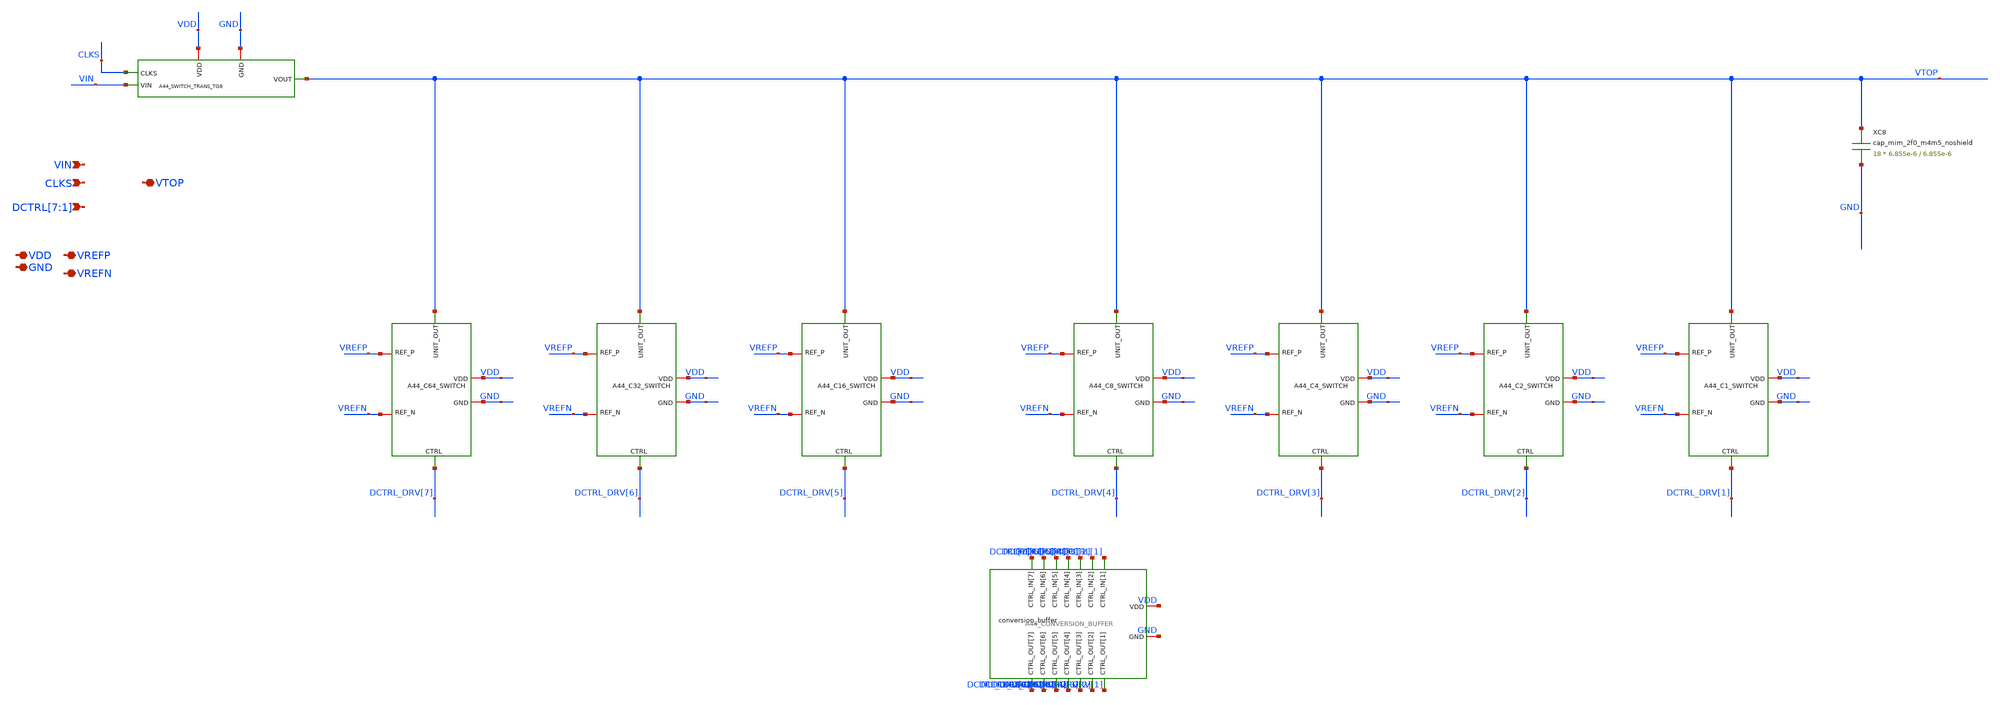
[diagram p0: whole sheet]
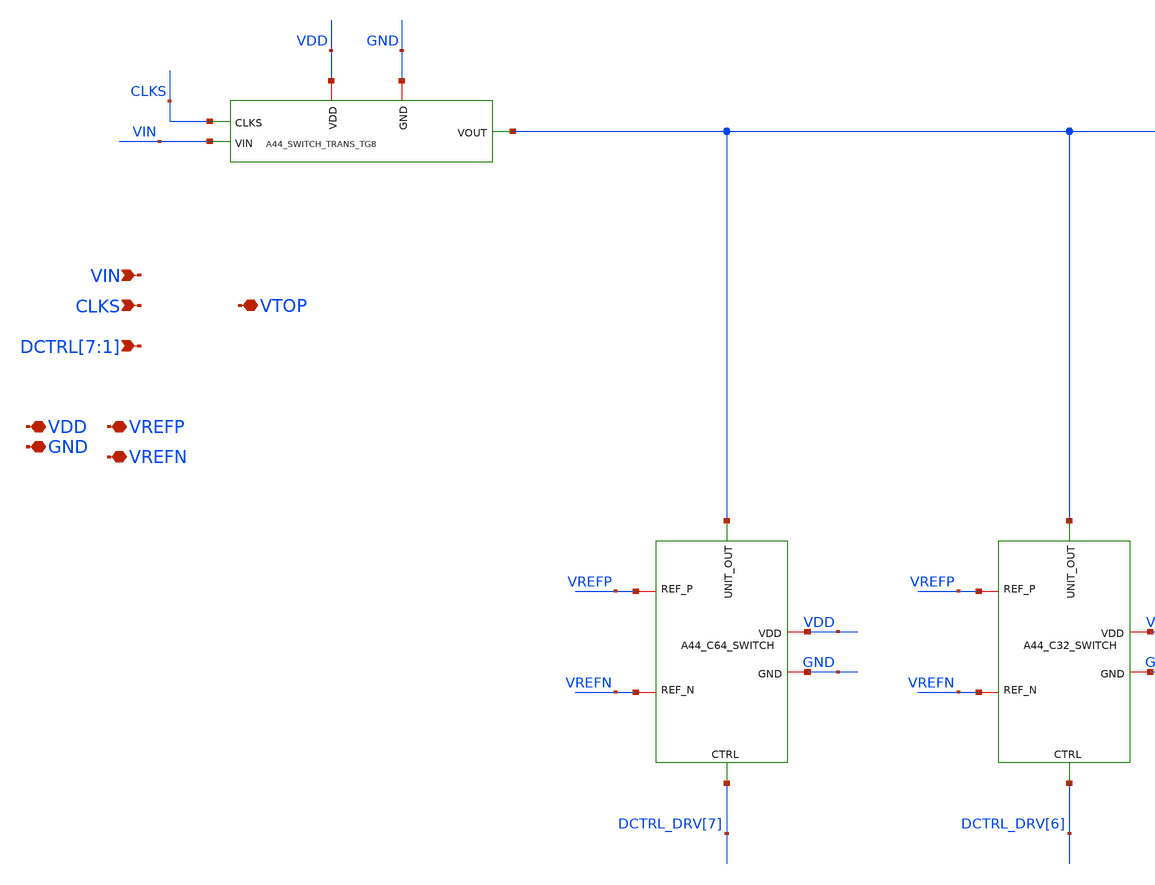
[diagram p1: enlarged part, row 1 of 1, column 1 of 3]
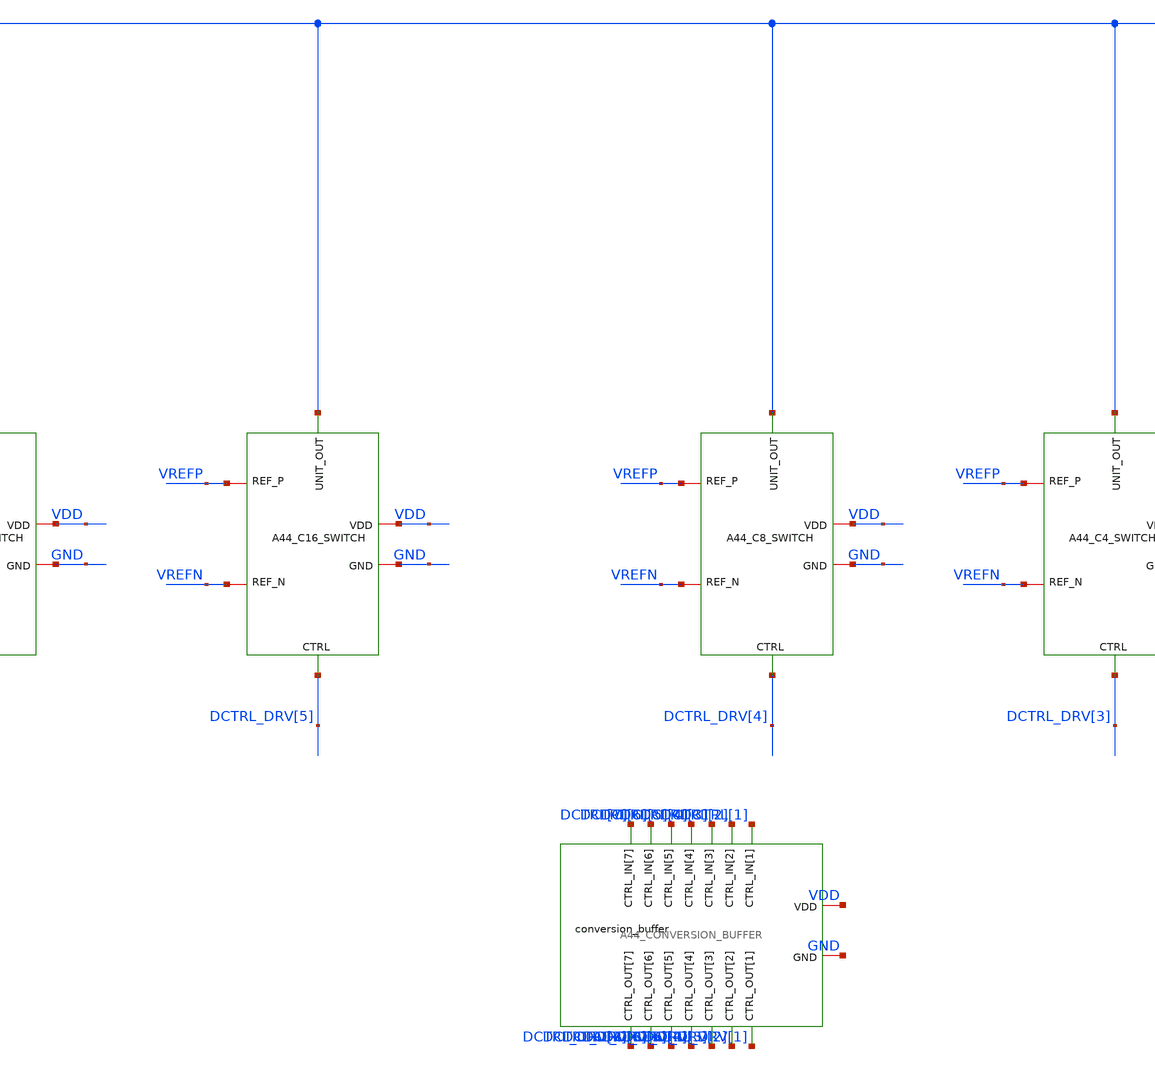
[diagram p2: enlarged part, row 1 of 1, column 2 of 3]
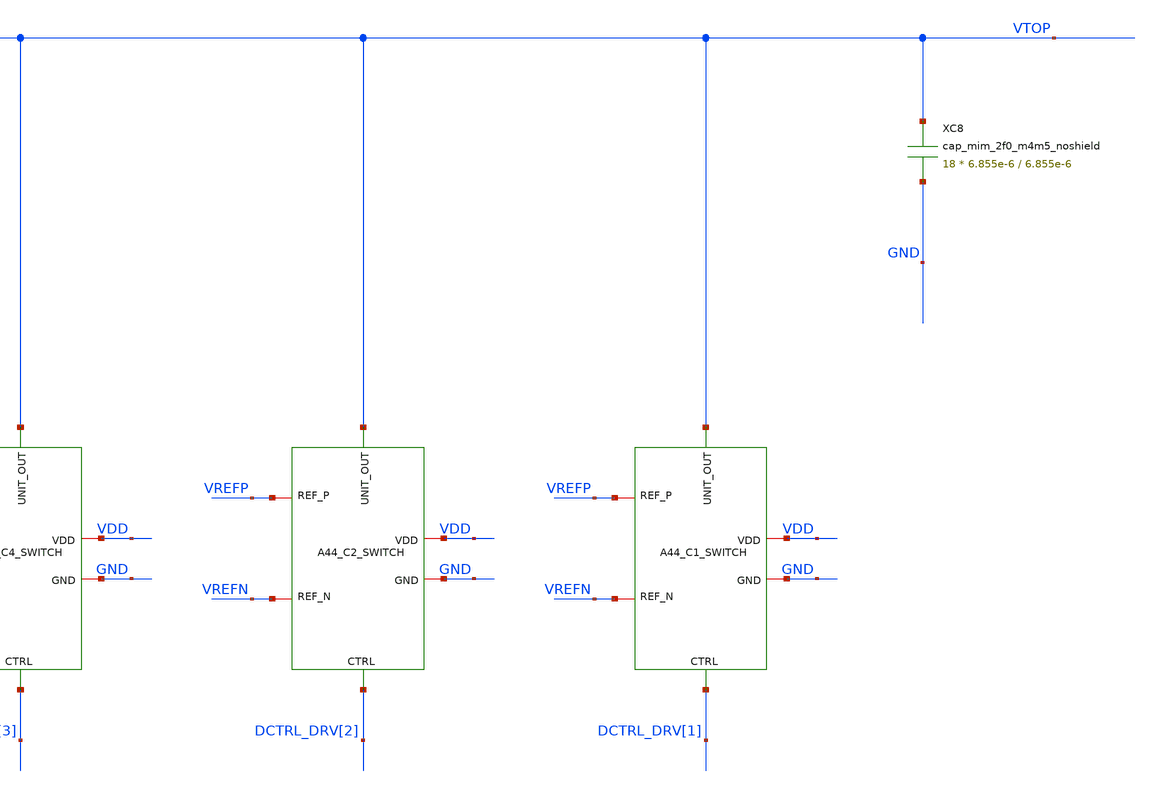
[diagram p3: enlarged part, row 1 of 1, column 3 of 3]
** sch_path: verification/a44_w5p29_trans_driver/01_CURRENT_CIRCUIT_FILES/xschem/A44_CDAC_UNIT_TRANS_DRIVER.sch
**.subckt A44_CDAC_UNIT_TRANS_DRIVER VIN CLKS VDD GND VREFP VREFN VTOP
*+ DCTRL[7],DCTRL[6],DCTRL[5],DCTRL[4],DCTRL[3],DCTRL[2],DCTRL[1]
*.ipin VIN
*.ipin CLKS
*.iopin VDD
*.iopin GND
*.iopin VREFP
*.iopin VREFN
*.iopin VTOP
*.ipin DCTRL[7],DCTRL[6],DCTRL[5],DCTRL[4],DCTRL[3],DCTRL[2],DCTRL[1]
XC8 VTOP GND cap_mim_2f0_m4m5_noshield c_width=6.855e-6 c_length=6.855e-6 m=18
x2 VREFN VREFP VDD GND VTOP DCTRL_DRV[1] A44_C1_SWITCH
x3 VREFN VREFP VDD GND VTOP DCTRL_DRV[2] A44_C2_SWITCH
x4 VREFN VREFP VDD GND VTOP DCTRL_DRV[3] A44_C4_SWITCH
x5 VREFN VREFP VDD GND VTOP DCTRL_DRV[4] A44_C8_SWITCH
x6 VREFN VREFP VDD GND VTOP DCTRL_DRV[5] A44_C16_SWITCH
x8 VREFN VREFP VDD GND VTOP DCTRL_DRV[7] A44_C64_SWITCH
xsample CLKS VDD GND VTOP VIN A44_SWITCH_TRANS_TG8
x1 VREFN VREFP VDD GND VTOP DCTRL_DRV[6] A44_C32_SWITCH
xdrv DCTRL[1] DCTRL_DRV[1] VDD GND DCTRL[2] DCTRL_DRV[2] DCTRL_DRV[3] DCTRL[3] DCTRL_DRV[4] DCTRL[4]
+ DCTRL_DRV[5] DCTRL[5] DCTRL_DRV[6] DCTRL[6] DCTRL_DRV[7] DCTRL[7] A44_CONVERSION_BUFFER
**.ends

* expanding   symbol:  A44_C1_SWITCH.sym # of pins=6
** sym_path: verification/a44_w5p29_trans_driver/01_CURRENT_CIRCUIT_FILES/xschem/A44_C1_SWITCH.sym
** sch_path: verification/a44_w5p29_trans_driver/01_CURRENT_CIRCUIT_FILES/xschem/A44_C1_SWITCH.sch
.subckt A44_C1_SWITCH REF_N REF_P VDD GND UNIT_OUT CTRL
*.iopin REF_N
*.iopin REF_P
*.iopin VDD
*.iopin GND
*.ipin CTRL
*.opin UNIT_OUT
x1 REF_P REF_N CTRL V_BOT VDD GND A44_CAP_SWITCH
XC1 UNIT_OUT V_BOT cap_mim_2f0_m4m5_noshield c_width=6.855e-6 c_length=6.855e-6 m=18
.ends


* expanding   symbol:  A44_C2_SWITCH.sym # of pins=6
** sym_path: verification/a44_w5p29_trans_driver/01_CURRENT_CIRCUIT_FILES/xschem/A44_C2_SWITCH.sym
** sch_path: verification/a44_w5p29_trans_driver/01_CURRENT_CIRCUIT_FILES/xschem/A44_C2_SWITCH.sch
.subckt A44_C2_SWITCH REF_N REF_P VDD GND UNIT_OUT CTRL
*.iopin REF_N
*.iopin REF_P
*.iopin VDD
*.iopin GND
*.ipin CTRL
*.opin UNIT_OUT
x1 REF_N REF_P VDD GND UNIT_OUT CTRL A44_C1_SWITCH
x2 REF_N REF_P VDD GND UNIT_OUT CTRL A44_C1_SWITCH
.ends


* expanding   symbol:  A44_C4_SWITCH.sym # of pins=6
** sym_path: verification/a44_w5p29_trans_driver/01_CURRENT_CIRCUIT_FILES/xschem/A44_C4_SWITCH.sym
** sch_path: verification/a44_w5p29_trans_driver/01_CURRENT_CIRCUIT_FILES/xschem/A44_C4_SWITCH.sch
.subckt A44_C4_SWITCH REF_N REF_P VDD GND UNIT_OUT CTRL
*.iopin REF_N
*.iopin REF_P
*.iopin VDD
*.iopin GND
*.ipin CTRL
*.opin UNIT_OUT
x1 REF_N REF_P VDD GND UNIT_OUT CTRL A44_C1_SWITCH
x2 REF_N REF_P VDD GND UNIT_OUT CTRL A44_C1_SWITCH
x3 REF_N REF_P VDD GND UNIT_OUT CTRL A44_C1_SWITCH
x4 REF_N REF_P VDD GND UNIT_OUT CTRL A44_C1_SWITCH
.ends


* expanding   symbol:  A44_C8_SWITCH.sym # of pins=6
** sym_path: verification/a44_w5p29_trans_driver/01_CURRENT_CIRCUIT_FILES/xschem/A44_C8_SWITCH.sym
** sch_path: verification/a44_w5p29_trans_driver/01_CURRENT_CIRCUIT_FILES/xschem/A44_C8_SWITCH.sch
.subckt A44_C8_SWITCH REF_N REF_P VDD GND UNIT_OUT CTRL
*.iopin REF_N
*.iopin REF_P
*.iopin VDD
*.iopin GND
*.ipin CTRL
*.opin UNIT_OUT
x1 REF_N REF_P VDD GND UNIT_OUT CTRL A44_C1_SWITCH
x2 REF_N REF_P VDD GND UNIT_OUT CTRL A44_C1_SWITCH
x3 REF_N REF_P VDD GND UNIT_OUT CTRL A44_C1_SWITCH
x4 REF_N REF_P VDD GND UNIT_OUT CTRL A44_C1_SWITCH
x5 REF_N REF_P VDD GND UNIT_OUT CTRL A44_C1_SWITCH
x6 REF_N REF_P VDD GND UNIT_OUT CTRL A44_C1_SWITCH
x7 REF_N REF_P VDD GND UNIT_OUT CTRL A44_C1_SWITCH
x8 REF_N REF_P VDD GND UNIT_OUT CTRL A44_C1_SWITCH
.ends


* expanding   symbol:  A44_C16_SWITCH.sym # of pins=6
** sym_path: verification/a44_w5p29_trans_driver/01_CURRENT_CIRCUIT_FILES/xschem/A44_C16_SWITCH.sym
** sch_path: verification/a44_w5p29_trans_driver/01_CURRENT_CIRCUIT_FILES/xschem/A44_C16_SWITCH.sch
.subckt A44_C16_SWITCH REF_N REF_P VDD GND UNIT_OUT CTRL
*.iopin REF_N
*.iopin REF_P
*.iopin VDD
*.iopin GND
*.ipin CTRL
*.opin UNIT_OUT
x1 REF_N REF_P VDD GND UNIT_OUT CTRL A44_C1_SWITCH
x2 REF_N REF_P VDD GND UNIT_OUT CTRL A44_C1_SWITCH
x3 REF_N REF_P VDD GND UNIT_OUT CTRL A44_C1_SWITCH
x4 REF_N REF_P VDD GND UNIT_OUT CTRL A44_C1_SWITCH
x5 REF_N REF_P VDD GND UNIT_OUT CTRL A44_C1_SWITCH
x6 REF_N REF_P VDD GND UNIT_OUT CTRL A44_C1_SWITCH
x7 REF_N REF_P VDD GND UNIT_OUT CTRL A44_C1_SWITCH
x8 REF_N REF_P VDD GND UNIT_OUT CTRL A44_C1_SWITCH
x9 REF_N REF_P VDD GND UNIT_OUT CTRL A44_C1_SWITCH
x10 REF_N REF_P VDD GND UNIT_OUT CTRL A44_C1_SWITCH
x11 REF_N REF_P VDD GND UNIT_OUT CTRL A44_C1_SWITCH
x12 REF_N REF_P VDD GND UNIT_OUT CTRL A44_C1_SWITCH
x13 REF_N REF_P VDD GND UNIT_OUT CTRL A44_C1_SWITCH
x14 REF_N REF_P VDD GND UNIT_OUT CTRL A44_C1_SWITCH
x15 REF_N REF_P VDD GND UNIT_OUT CTRL A44_C1_SWITCH
x16 REF_N REF_P VDD GND UNIT_OUT CTRL A44_C1_SWITCH
.ends


* expanding   symbol:  A44_C64_SWITCH.sym # of pins=6
** sym_path: verification/a44_w5p29_trans_driver/01_CURRENT_CIRCUIT_FILES/xschem/A44_C64_SWITCH.sym
** sch_path: verification/a44_w5p29_trans_driver/01_CURRENT_CIRCUIT_FILES/xschem/A44_C64_SWITCH.sch
.subckt A44_C64_SWITCH REF_N REF_P VDD GND UNIT_OUT CTRL
*.iopin REF_N
*.iopin REF_P
*.iopin VDD
*.iopin GND
*.ipin CTRL
*.opin UNIT_OUT
x1 REF_N REF_P VDD GND UNIT_OUT CTRL A44_C1_SWITCH
x2 REF_N REF_P VDD GND UNIT_OUT CTRL A44_C1_SWITCH
x3 REF_N REF_P VDD GND UNIT_OUT CTRL A44_C1_SWITCH
x4 REF_N REF_P VDD GND UNIT_OUT CTRL A44_C1_SWITCH
x5 REF_N REF_P VDD GND UNIT_OUT CTRL A44_C1_SWITCH
x6 REF_N REF_P VDD GND UNIT_OUT CTRL A44_C1_SWITCH
x7 REF_N REF_P VDD GND UNIT_OUT CTRL A44_C1_SWITCH
x8 REF_N REF_P VDD GND UNIT_OUT CTRL A44_C1_SWITCH
x9 REF_N REF_P VDD GND UNIT_OUT CTRL A44_C1_SWITCH
x10 REF_N REF_P VDD GND UNIT_OUT CTRL A44_C1_SWITCH
x11 REF_N REF_P VDD GND UNIT_OUT CTRL A44_C1_SWITCH
x12 REF_N REF_P VDD GND UNIT_OUT CTRL A44_C1_SWITCH
x13 REF_N REF_P VDD GND UNIT_OUT CTRL A44_C1_SWITCH
x14 REF_N REF_P VDD GND UNIT_OUT CTRL A44_C1_SWITCH
x15 REF_N REF_P VDD GND UNIT_OUT CTRL A44_C1_SWITCH
x16 REF_N REF_P VDD GND UNIT_OUT CTRL A44_C1_SWITCH
x17 REF_N REF_P VDD GND UNIT_OUT CTRL A44_C1_SWITCH
x18 REF_N REF_P VDD GND UNIT_OUT CTRL A44_C1_SWITCH
x19 REF_N REF_P VDD GND UNIT_OUT CTRL A44_C1_SWITCH
x20 REF_N REF_P VDD GND UNIT_OUT CTRL A44_C1_SWITCH
x21 REF_N REF_P VDD GND UNIT_OUT CTRL A44_C1_SWITCH
x22 REF_N REF_P VDD GND UNIT_OUT CTRL A44_C1_SWITCH
x23 REF_N REF_P VDD GND UNIT_OUT CTRL A44_C1_SWITCH
x24 REF_N REF_P VDD GND UNIT_OUT CTRL A44_C1_SWITCH
x25 REF_N REF_P VDD GND UNIT_OUT CTRL A44_C1_SWITCH
x26 REF_N REF_P VDD GND UNIT_OUT CTRL A44_C1_SWITCH
x27 REF_N REF_P VDD GND UNIT_OUT CTRL A44_C1_SWITCH
x28 REF_N REF_P VDD GND UNIT_OUT CTRL A44_C1_SWITCH
x29 REF_N REF_P VDD GND UNIT_OUT CTRL A44_C1_SWITCH
x30 REF_N REF_P VDD GND UNIT_OUT CTRL A44_C1_SWITCH
x31 REF_N REF_P VDD GND UNIT_OUT CTRL A44_C1_SWITCH
x32 REF_N REF_P VDD GND UNIT_OUT CTRL A44_C1_SWITCH
x33 REF_N REF_P VDD GND UNIT_OUT CTRL A44_C1_SWITCH
x34 REF_N REF_P VDD GND UNIT_OUT CTRL A44_C1_SWITCH
x35 REF_N REF_P VDD GND UNIT_OUT CTRL A44_C1_SWITCH
x36 REF_N REF_P VDD GND UNIT_OUT CTRL A44_C1_SWITCH
x37 REF_N REF_P VDD GND UNIT_OUT CTRL A44_C1_SWITCH
x38 REF_N REF_P VDD GND UNIT_OUT CTRL A44_C1_SWITCH
x39 REF_N REF_P VDD GND UNIT_OUT CTRL A44_C1_SWITCH
x40 REF_N REF_P VDD GND UNIT_OUT CTRL A44_C1_SWITCH
x41 REF_N REF_P VDD GND UNIT_OUT CTRL A44_C1_SWITCH
x42 REF_N REF_P VDD GND UNIT_OUT CTRL A44_C1_SWITCH
x43 REF_N REF_P VDD GND UNIT_OUT CTRL A44_C1_SWITCH
x44 REF_N REF_P VDD GND UNIT_OUT CTRL A44_C1_SWITCH
x45 REF_N REF_P VDD GND UNIT_OUT CTRL A44_C1_SWITCH
x46 REF_N REF_P VDD GND UNIT_OUT CTRL A44_C1_SWITCH
x47 REF_N REF_P VDD GND UNIT_OUT CTRL A44_C1_SWITCH
x48 REF_N REF_P VDD GND UNIT_OUT CTRL A44_C1_SWITCH
x49 REF_N REF_P VDD GND UNIT_OUT CTRL A44_C1_SWITCH
x50 REF_N REF_P VDD GND UNIT_OUT CTRL A44_C1_SWITCH
x51 REF_N REF_P VDD GND UNIT_OUT CTRL A44_C1_SWITCH
x52 REF_N REF_P VDD GND UNIT_OUT CTRL A44_C1_SWITCH
x53 REF_N REF_P VDD GND UNIT_OUT CTRL A44_C1_SWITCH
x54 REF_N REF_P VDD GND UNIT_OUT CTRL A44_C1_SWITCH
x55 REF_N REF_P VDD GND UNIT_OUT CTRL A44_C1_SWITCH
x56 REF_N REF_P VDD GND UNIT_OUT CTRL A44_C1_SWITCH
x57 REF_N REF_P VDD GND UNIT_OUT CTRL A44_C1_SWITCH
x58 REF_N REF_P VDD GND UNIT_OUT CTRL A44_C1_SWITCH
x59 REF_N REF_P VDD GND UNIT_OUT CTRL A44_C1_SWITCH
x60 REF_N REF_P VDD GND UNIT_OUT CTRL A44_C1_SWITCH
x61 REF_N REF_P VDD GND UNIT_OUT CTRL A44_C1_SWITCH
x62 REF_N REF_P VDD GND UNIT_OUT CTRL A44_C1_SWITCH
x63 REF_N REF_P VDD GND UNIT_OUT CTRL A44_C1_SWITCH
x64 REF_N REF_P VDD GND UNIT_OUT CTRL A44_C1_SWITCH
.ends


* expanding   symbol:  A44_SWITCH_TRANS_TG8.sym # of pins=5
** sym_path: verification/a44_w5p29_trans_driver/01_CURRENT_CIRCUIT_FILES/xschem/A44_SWITCH_TRANS_TG8.sym
** sch_path: verification/a44_w5p29_trans_driver/01_CURRENT_CIRCUIT_FILES/xschem/A44_SWITCH_TRANS_TG8.sch
.subckt A44_SWITCH_TRANS_TG8 CLKS VDD GND VOUT VIN
*.iopin VDD
*.iopin GND
*.ipin VIN
*.ipin CLKS
*.opin VOUT
XTG_CLK_INV1_NMOS net1 CLKS GND GND nfet_03v3 L=0.28u W=1.56u nf=1 ad='int((nf+1)/2) * W/nf * 0.18u'
+ as='int((nf+2)/2) * W/nf * 0.18u' pd='2*int((nf+1)/2) * (W/nf + 0.18u)' ps='2*int((nf+2)/2) * (W/nf + 0.18u)'
+ nrd='0.18u / W' nrs='0.18u / W' sa=0 sb=0 sd=0 m=1
XTG_CLK_INV1_PMOS net1 CLKS VDD VDD pfet_03v3 L=0.28u W=3.11u nf=1 ad='int((nf+1)/2) * W/nf * 0.18u'
+ as='int((nf+2)/2) * W/nf * 0.18u' pd='2*int((nf+1)/2) * (W/nf + 0.18u)' ps='2*int((nf+2)/2) * (W/nf + 0.18u)'
+ nrd='0.18u / W' nrs='0.18u / W' sa=0 sb=0 sd=0 m=1
XTG_CLK_INV2_NMOS net2 net1 GND GND nfet_03v3 L=0.28u W=2.34u nf=1 ad='int((nf+1)/2) * W/nf * 0.18u'
+ as='int((nf+2)/2) * W/nf * 0.18u' pd='2*int((nf+1)/2) * (W/nf + 0.18u)' ps='2*int((nf+2)/2) * (W/nf + 0.18u)'
+ nrd='0.18u / W' nrs='0.18u / W' sa=0 sb=0 sd=0 m=1
XTG_CLK_INV2_PMOS net2 net1 VDD VDD pfet_03v3 L=0.28u W=4.67u nf=1 ad='int((nf+1)/2) * W/nf * 0.18u'
+ as='int((nf+2)/2) * W/nf * 0.18u' pd='2*int((nf+1)/2) * (W/nf + 0.18u)' ps='2*int((nf+2)/2) * (W/nf + 0.18u)'
+ nrd='0.18u / W' nrs='0.18u / W' sa=0 sb=0 sd=0 m=1
XTG_CLK_INV3_NMOS net3 net2 GND GND nfet_03v3 L=0.28u W=3.11u nf=1 ad='int((nf+1)/2) * W/nf * 0.18u'
+ as='int((nf+2)/2) * W/nf * 0.18u' pd='2*int((nf+1)/2) * (W/nf + 0.18u)' ps='2*int((nf+2)/2) * (W/nf + 0.18u)'
+ nrd='0.18u / W' nrs='0.18u / W' sa=0 sb=0 sd=0 m=1
XTG_CLK_INV3_PMOS net3 net2 VDD VDD pfet_03v3 L=0.28u W=6.22u nf=1 ad='int((nf+1)/2) * W/nf * 0.18u'
+ as='int((nf+2)/2) * W/nf * 0.18u' pd='2*int((nf+1)/2) * (W/nf + 0.18u)' ps='2*int((nf+2)/2) * (W/nf + 0.18u)'
+ nrd='0.18u / W' nrs='0.18u / W' sa=0 sb=0 sd=0 m=1
XTG_CLK_INV4_NMOS N_CLK net3 GND GND nfet_03v3 L=0.28u W=4.67u nf=1 ad='int((nf+1)/2) * W/nf * 0.18u'
+ as='int((nf+2)/2) * W/nf * 0.18u' pd='2*int((nf+1)/2) * (W/nf + 0.18u)' ps='2*int((nf+2)/2) * (W/nf + 0.18u)'
+ nrd='0.18u / W' nrs='0.18u / W' sa=0 sb=0 sd=0 m=1
XTG_CLK_INV4_PMOS N_CLK net3 VDD VDD pfet_03v3 L=0.28u W=9.33u nf=1 ad='int((nf+1)/2) * W/nf * 0.18u'
+ as='int((nf+2)/2) * W/nf * 0.18u' pd='2*int((nf+1)/2) * (W/nf + 0.18u)' ps='2*int((nf+2)/2) * (W/nf + 0.18u)'
+ nrd='0.18u / W' nrs='0.18u / W' sa=0 sb=0 sd=0 m=1
XTG_PCLK_INV1_NMOS net4 CLKS GND GND nfet_03v3 L=0.28u W=1.56u nf=1 ad='int((nf+1)/2) * W/nf * 0.18u'
+ as='int((nf+2)/2) * W/nf * 0.18u' pd='2*int((nf+1)/2) * (W/nf + 0.18u)' ps='2*int((nf+2)/2) * (W/nf + 0.18u)'
+ nrd='0.18u / W' nrs='0.18u / W' sa=0 sb=0 sd=0 m=1
XTG_PCLK_INV1_PMOS net4 CLKS VDD VDD pfet_03v3 L=0.28u W=3.11u nf=1 ad='int((nf+1)/2) * W/nf * 0.18u'
+ as='int((nf+2)/2) * W/nf * 0.18u' pd='2*int((nf+1)/2) * (W/nf + 0.18u)' ps='2*int((nf+2)/2) * (W/nf + 0.18u)'
+ nrd='0.18u / W' nrs='0.18u / W' sa=0 sb=0 sd=0 m=1
XTG_PCLK_INV2_NMOS net5 net4 GND GND nfet_03v3 L=0.28u W=3.11u nf=1 ad='int((nf+1)/2) * W/nf * 0.18u'
+ as='int((nf+2)/2) * W/nf * 0.18u' pd='2*int((nf+1)/2) * (W/nf + 0.18u)' ps='2*int((nf+2)/2) * (W/nf + 0.18u)'
+ nrd='0.18u / W' nrs='0.18u / W' sa=0 sb=0 sd=0 m=1
XTG_PCLK_INV2_PMOS net5 net4 VDD VDD pfet_03v3 L=0.28u W=6.22u nf=1 ad='int((nf+1)/2) * W/nf * 0.18u'
+ as='int((nf+2)/2) * W/nf * 0.18u' pd='2*int((nf+1)/2) * (W/nf + 0.18u)' ps='2*int((nf+2)/2) * (W/nf + 0.18u)'
+ nrd='0.18u / W' nrs='0.18u / W' sa=0 sb=0 sd=0 m=1
XTG_PCLK_INV3_NMOS P_CLK net5 GND GND nfet_03v3 L=0.28u W=6.22u nf=1 ad='int((nf+1)/2) * W/nf * 0.18u'
+ as='int((nf+2)/2) * W/nf * 0.18u' pd='2*int((nf+1)/2) * (W/nf + 0.18u)' ps='2*int((nf+2)/2) * (W/nf + 0.18u)'
+ nrd='0.18u / W' nrs='0.18u / W' sa=0 sb=0 sd=0 m=1
XTG_PCLK_INV3_PMOS P_CLK net5 VDD VDD pfet_03v3 L=0.28u W=12.44u nf=1 ad='int((nf+1)/2) * W/nf * 0.18u'
+ as='int((nf+2)/2) * W/nf * 0.18u' pd='2*int((nf+1)/2) * (W/nf + 0.18u)' ps='2*int((nf+2)/2) * (W/nf + 0.18u)'
+ nrd='0.18u / W' nrs='0.18u / W' sa=0 sb=0 sd=0 m=1
XTG_TRANS_NMOS VIN N_CLK VOUT GND nfet_03v3 L=0.28u W=3.11u nf=1 ad='int((nf+1)/2) * W/nf * 0.18u' as='int((nf+2)/2) * W/nf * 0.18u'
+ pd='2*int((nf+1)/2) * (W/nf + 0.18u)' ps='2*int((nf+2)/2) * (W/nf + 0.18u)' nrd='0.18u / W' nrs='0.18u / W'
+ sa=0 sb=0 sd=0 m=8
XTG_TRANS_PMOS VIN P_CLK VOUT VDD pfet_03v3 L=0.28u W=6.22u nf=1 ad='int((nf+1)/2) * W/nf * 0.18u' as='int((nf+2)/2) * W/nf * 0.18u'
+ pd='2*int((nf+1)/2) * (W/nf + 0.18u)' ps='2*int((nf+2)/2) * (W/nf + 0.18u)' nrd='0.18u / W' nrs='0.18u / W'
+ sa=0 sb=0 sd=0 m=8
.ends


* expanding   symbol:  A44_C32_SWITCH.sym # of pins=6
** sym_path: verification/a44_w5p29_trans_driver/01_CURRENT_CIRCUIT_FILES/xschem/A44_C32_SWITCH.sym
** sch_path: verification/a44_w5p29_trans_driver/01_CURRENT_CIRCUIT_FILES/xschem/A44_C32_SWITCH.sch
.subckt A44_C32_SWITCH REF_N REF_P VDD GND UNIT_OUT CTRL
*.iopin REF_N
*.iopin REF_P
*.iopin VDD
*.iopin GND
*.ipin CTRL
*.opin UNIT_OUT
x1 REF_N REF_P VDD GND UNIT_OUT CTRL A44_C1_SWITCH
x2 REF_N REF_P VDD GND UNIT_OUT CTRL A44_C1_SWITCH
x3 REF_N REF_P VDD GND UNIT_OUT CTRL A44_C1_SWITCH
x4 REF_N REF_P VDD GND UNIT_OUT CTRL A44_C1_SWITCH
x5 REF_N REF_P VDD GND UNIT_OUT CTRL A44_C1_SWITCH
x6 REF_N REF_P VDD GND UNIT_OUT CTRL A44_C1_SWITCH
x7 REF_N REF_P VDD GND UNIT_OUT CTRL A44_C1_SWITCH
x8 REF_N REF_P VDD GND UNIT_OUT CTRL A44_C1_SWITCH
x9 REF_N REF_P VDD GND UNIT_OUT CTRL A44_C1_SWITCH
x10 REF_N REF_P VDD GND UNIT_OUT CTRL A44_C1_SWITCH
x11 REF_N REF_P VDD GND UNIT_OUT CTRL A44_C1_SWITCH
x12 REF_N REF_P VDD GND UNIT_OUT CTRL A44_C1_SWITCH
x13 REF_N REF_P VDD GND UNIT_OUT CTRL A44_C1_SWITCH
x14 REF_N REF_P VDD GND UNIT_OUT CTRL A44_C1_SWITCH
x15 REF_N REF_P VDD GND UNIT_OUT CTRL A44_C1_SWITCH
x16 REF_N REF_P VDD GND UNIT_OUT CTRL A44_C1_SWITCH
x17 REF_N REF_P VDD GND UNIT_OUT CTRL A44_C1_SWITCH
x18 REF_N REF_P VDD GND UNIT_OUT CTRL A44_C1_SWITCH
x19 REF_N REF_P VDD GND UNIT_OUT CTRL A44_C1_SWITCH
x20 REF_N REF_P VDD GND UNIT_OUT CTRL A44_C1_SWITCH
x21 REF_N REF_P VDD GND UNIT_OUT CTRL A44_C1_SWITCH
x22 REF_N REF_P VDD GND UNIT_OUT CTRL A44_C1_SWITCH
x23 REF_N REF_P VDD GND UNIT_OUT CTRL A44_C1_SWITCH
x24 REF_N REF_P VDD GND UNIT_OUT CTRL A44_C1_SWITCH
x25 REF_N REF_P VDD GND UNIT_OUT CTRL A44_C1_SWITCH
x26 REF_N REF_P VDD GND UNIT_OUT CTRL A44_C1_SWITCH
x27 REF_N REF_P VDD GND UNIT_OUT CTRL A44_C1_SWITCH
x28 REF_N REF_P VDD GND UNIT_OUT CTRL A44_C1_SWITCH
x29 REF_N REF_P VDD GND UNIT_OUT CTRL A44_C1_SWITCH
x30 REF_N REF_P VDD GND UNIT_OUT CTRL A44_C1_SWITCH
x31 REF_N REF_P VDD GND UNIT_OUT CTRL A44_C1_SWITCH
x32 REF_N REF_P VDD GND UNIT_OUT CTRL A44_C1_SWITCH
.ends


* expanding   symbol:  A44_CONVERSION_BUFFER.sym # of pins=16
** sym_path: verification/a44_w5p29_trans_driver/01_CURRENT_CIRCUIT_FILES/xschem/A44_CONVERSION_BUFFER.sym
** sch_path: verification/a44_w5p29_trans_driver/01_CURRENT_CIRCUIT_FILES/xschem/A44_CONVERSION_BUFFER.sch
.subckt A44_CONVERSION_BUFFER CTRL_IN[1] CTRL_OUT[1] VDD GND CTRL_IN[2] CTRL_OUT[2] CTRL_OUT[3]
+ CTRL_IN[3] CTRL_OUT[4] CTRL_IN[4] CTRL_OUT[5] CTRL_IN[5] CTRL_OUT[6] CTRL_IN[6] CTRL_OUT[7] CTRL_IN[7]
*.ipin CTRL_IN[2]
*.opin CTRL_OUT[2]
*.iopin VDD
*.iopin GND
*.ipin CTRL_IN[1]
*.opin CTRL_OUT[1]
*.ipin CTRL_IN[4]
*.opin CTRL_OUT[4]
*.ipin CTRL_IN[3]
*.opin CTRL_OUT[3]
*.ipin CTRL_IN[6]
*.opin CTRL_OUT[6]
*.ipin CTRL_IN[5]
*.opin CTRL_OUT[5]
*.ipin CTRL_IN[7]
*.opin CTRL_OUT[7]
XDCTRL_CH2_INV1_NMOS net1 CTRL_IN[2] GND GND nfet_03v3 L=0.28u W=2.34u nf=1 ad='int((nf+1)/2) * W/nf * 0.18u'
+ as='int((nf+2)/2) * W/nf * 0.18u' pd='2*int((nf+1)/2) * (W/nf + 0.18u)' ps='2*int((nf+2)/2) * (W/nf + 0.18u)'
+ nrd='0.18u / W' nrs='0.18u / W' sa=0 sb=0 sd=0 m=1
XDCTRL_CH2_INV1_PMOS net1 CTRL_IN[2] VDD VDD pfet_03v3 L=0.28u W=4.67u nf=1 ad='int((nf+1)/2) * W/nf * 0.18u'
+ as='int((nf+2)/2) * W/nf * 0.18u' pd='2*int((nf+1)/2) * (W/nf + 0.18u)' ps='2*int((nf+2)/2) * (W/nf + 0.18u)'
+ nrd='0.18u / W' nrs='0.18u / W' sa=0 sb=0 sd=0 m=1
XDCTRL_CH2_INV2_NMOS CTRL_OUT[2] net1 GND GND nfet_03v3 L=0.28u W=6.22u nf=1 ad='int((nf+1)/2) * W/nf * 0.18u'
+ as='int((nf+2)/2) * W/nf * 0.18u' pd='2*int((nf+1)/2) * (W/nf + 0.18u)' ps='2*int((nf+2)/2) * (W/nf + 0.18u)'
+ nrd='0.18u / W' nrs='0.18u / W' sa=0 sb=0 sd=0 m=1
XDCTRL_CH2_INV2_PMOS CTRL_OUT[2] net1 VDD VDD pfet_03v3 L=0.28u W=12.44u nf=1 ad='int((nf+1)/2) * W/nf * 0.18u'
+ as='int((nf+2)/2) * W/nf * 0.18u' pd='2*int((nf+1)/2) * (W/nf + 0.18u)' ps='2*int((nf+2)/2) * (W/nf + 0.18u)'
+ nrd='0.18u / W' nrs='0.18u / W' sa=0 sb=0 sd=0 m=1
XDCTRL_CH1_INV1_NMOS net2 CTRL_IN[1] GND GND nfet_03v3 L=0.28u W=2.34u nf=1 ad='int((nf+1)/2) * W/nf * 0.18u'
+ as='int((nf+2)/2) * W/nf * 0.18u' pd='2*int((nf+1)/2) * (W/nf + 0.18u)' ps='2*int((nf+2)/2) * (W/nf + 0.18u)'
+ nrd='0.18u / W' nrs='0.18u / W' sa=0 sb=0 sd=0 m=1
XDCTRL_CH1_INV1_PMOS net2 CTRL_IN[1] VDD VDD pfet_03v3 L=0.28u W=4.67u nf=1 ad='int((nf+1)/2) * W/nf * 0.18u'
+ as='int((nf+2)/2) * W/nf * 0.18u' pd='2*int((nf+1)/2) * (W/nf + 0.18u)' ps='2*int((nf+2)/2) * (W/nf + 0.18u)'
+ nrd='0.18u / W' nrs='0.18u / W' sa=0 sb=0 sd=0 m=1
XDCTRL_CH1_INV2_NMOS CTRL_OUT[1] net2 GND GND nfet_03v3 L=0.28u W=6.22u nf=1 ad='int((nf+1)/2) * W/nf * 0.18u'
+ as='int((nf+2)/2) * W/nf * 0.18u' pd='2*int((nf+1)/2) * (W/nf + 0.18u)' ps='2*int((nf+2)/2) * (W/nf + 0.18u)'
+ nrd='0.18u / W' nrs='0.18u / W' sa=0 sb=0 sd=0 m=1
XDCTRL_CH1_INV2_PMOS CTRL_OUT[1] net2 VDD VDD pfet_03v3 L=0.28u W=12.44u nf=1 ad='int((nf+1)/2) * W/nf * 0.18u'
+ as='int((nf+2)/2) * W/nf * 0.18u' pd='2*int((nf+1)/2) * (W/nf + 0.18u)' ps='2*int((nf+2)/2) * (W/nf + 0.18u)'
+ nrd='0.18u / W' nrs='0.18u / W' sa=0 sb=0 sd=0 m=1
XDCTRL_CH4_INV1_NMOS net3 CTRL_IN[4] GND GND nfet_03v3 L=0.28u W=2.34u nf=1 ad='int((nf+1)/2) * W/nf * 0.18u'
+ as='int((nf+2)/2) * W/nf * 0.18u' pd='2*int((nf+1)/2) * (W/nf + 0.18u)' ps='2*int((nf+2)/2) * (W/nf + 0.18u)'
+ nrd='0.18u / W' nrs='0.18u / W' sa=0 sb=0 sd=0 m=1
XDCTRL_CH4_INV1_PMOS net3 CTRL_IN[4] VDD VDD pfet_03v3 L=0.28u W=4.67u nf=1 ad='int((nf+1)/2) * W/nf * 0.18u'
+ as='int((nf+2)/2) * W/nf * 0.18u' pd='2*int((nf+1)/2) * (W/nf + 0.18u)' ps='2*int((nf+2)/2) * (W/nf + 0.18u)'
+ nrd='0.18u / W' nrs='0.18u / W' sa=0 sb=0 sd=0 m=1
XDCTRL_CH4_INV2_NMOS CTRL_OUT[4] net3 GND GND nfet_03v3 L=0.28u W=6.22u nf=1 ad='int((nf+1)/2) * W/nf * 0.18u'
+ as='int((nf+2)/2) * W/nf * 0.18u' pd='2*int((nf+1)/2) * (W/nf + 0.18u)' ps='2*int((nf+2)/2) * (W/nf + 0.18u)'
+ nrd='0.18u / W' nrs='0.18u / W' sa=0 sb=0 sd=0 m=1
XDCTRL_CH4_INV2_PMOS CTRL_OUT[4] net3 VDD VDD pfet_03v3 L=0.28u W=12.44u nf=1 ad='int((nf+1)/2) * W/nf * 0.18u'
+ as='int((nf+2)/2) * W/nf * 0.18u' pd='2*int((nf+1)/2) * (W/nf + 0.18u)' ps='2*int((nf+2)/2) * (W/nf + 0.18u)'
+ nrd='0.18u / W' nrs='0.18u / W' sa=0 sb=0 sd=0 m=1
XDCTRL_CH3_INV1_NMOS net4 CTRL_IN[3] GND GND nfet_03v3 L=0.28u W=2.34u nf=1 ad='int((nf+1)/2) * W/nf * 0.18u'
+ as='int((nf+2)/2) * W/nf * 0.18u' pd='2*int((nf+1)/2) * (W/nf + 0.18u)' ps='2*int((nf+2)/2) * (W/nf + 0.18u)'
+ nrd='0.18u / W' nrs='0.18u / W' sa=0 sb=0 sd=0 m=1
XDCTRL_CH3_INV1_PMOS net4 CTRL_IN[3] VDD VDD pfet_03v3 L=0.28u W=4.67u nf=1 ad='int((nf+1)/2) * W/nf * 0.18u'
+ as='int((nf+2)/2) * W/nf * 0.18u' pd='2*int((nf+1)/2) * (W/nf + 0.18u)' ps='2*int((nf+2)/2) * (W/nf + 0.18u)'
+ nrd='0.18u / W' nrs='0.18u / W' sa=0 sb=0 sd=0 m=1
XDCTRL_CH3_INV2_NMOS CTRL_OUT[3] net4 GND GND nfet_03v3 L=0.28u W=6.22u nf=1 ad='int((nf+1)/2) * W/nf * 0.18u'
+ as='int((nf+2)/2) * W/nf * 0.18u' pd='2*int((nf+1)/2) * (W/nf + 0.18u)' ps='2*int((nf+2)/2) * (W/nf + 0.18u)'
+ nrd='0.18u / W' nrs='0.18u / W' sa=0 sb=0 sd=0 m=1
XDCTRL_CH3_INV2_PMOS CTRL_OUT[3] net4 VDD VDD pfet_03v3 L=0.28u W=12.44u nf=1 ad='int((nf+1)/2) * W/nf * 0.18u'
+ as='int((nf+2)/2) * W/nf * 0.18u' pd='2*int((nf+1)/2) * (W/nf + 0.18u)' ps='2*int((nf+2)/2) * (W/nf + 0.18u)'
+ nrd='0.18u / W' nrs='0.18u / W' sa=0 sb=0 sd=0 m=1
XDCTRL_CH6_INV1_NMOS net5 CTRL_IN[6] GND GND nfet_03v3 L=0.28u W=2.34u nf=1 ad='int((nf+1)/2) * W/nf * 0.18u'
+ as='int((nf+2)/2) * W/nf * 0.18u' pd='2*int((nf+1)/2) * (W/nf + 0.18u)' ps='2*int((nf+2)/2) * (W/nf + 0.18u)'
+ nrd='0.18u / W' nrs='0.18u / W' sa=0 sb=0 sd=0 m=1
XDCTRL_CH6_INV1_PMOS net5 CTRL_IN[6] VDD VDD pfet_03v3 L=0.28u W=4.67u nf=1 ad='int((nf+1)/2) * W/nf * 0.18u'
+ as='int((nf+2)/2) * W/nf * 0.18u' pd='2*int((nf+1)/2) * (W/nf + 0.18u)' ps='2*int((nf+2)/2) * (W/nf + 0.18u)'
+ nrd='0.18u / W' nrs='0.18u / W' sa=0 sb=0 sd=0 m=1
XDCTRL_CH6_INV2_NMOS CTRL_OUT[6] net5 GND GND nfet_03v3 L=0.28u W=6.22u nf=1 ad='int((nf+1)/2) * W/nf * 0.18u'
+ as='int((nf+2)/2) * W/nf * 0.18u' pd='2*int((nf+1)/2) * (W/nf + 0.18u)' ps='2*int((nf+2)/2) * (W/nf + 0.18u)'
+ nrd='0.18u / W' nrs='0.18u / W' sa=0 sb=0 sd=0 m=1
XDCTRL_CH6_INV2_PMOS CTRL_OUT[6] net5 VDD VDD pfet_03v3 L=0.28u W=12.44u nf=1 ad='int((nf+1)/2) * W/nf * 0.18u'
+ as='int((nf+2)/2) * W/nf * 0.18u' pd='2*int((nf+1)/2) * (W/nf + 0.18u)' ps='2*int((nf+2)/2) * (W/nf + 0.18u)'
+ nrd='0.18u / W' nrs='0.18u / W' sa=0 sb=0 sd=0 m=1
XDCTRL_CH5_INV1_NMOS net6 CTRL_IN[5] GND GND nfet_03v3 L=0.28u W=2.34u nf=1 ad='int((nf+1)/2) * W/nf * 0.18u'
+ as='int((nf+2)/2) * W/nf * 0.18u' pd='2*int((nf+1)/2) * (W/nf + 0.18u)' ps='2*int((nf+2)/2) * (W/nf + 0.18u)'
+ nrd='0.18u / W' nrs='0.18u / W' sa=0 sb=0 sd=0 m=1
XDCTRL_CH5_INV1_PMOS net6 CTRL_IN[5] VDD VDD pfet_03v3 L=0.28u W=4.67u nf=1 ad='int((nf+1)/2) * W/nf * 0.18u'
+ as='int((nf+2)/2) * W/nf * 0.18u' pd='2*int((nf+1)/2) * (W/nf + 0.18u)' ps='2*int((nf+2)/2) * (W/nf + 0.18u)'
+ nrd='0.18u / W' nrs='0.18u / W' sa=0 sb=0 sd=0 m=1
XDCTRL_CH5_INV2_NMOS CTRL_OUT[5] net6 GND GND nfet_03v3 L=0.28u W=6.22u nf=1 ad='int((nf+1)/2) * W/nf * 0.18u'
+ as='int((nf+2)/2) * W/nf * 0.18u' pd='2*int((nf+1)/2) * (W/nf + 0.18u)' ps='2*int((nf+2)/2) * (W/nf + 0.18u)'
+ nrd='0.18u / W' nrs='0.18u / W' sa=0 sb=0 sd=0 m=1
XDCTRL_CH5_INV2_PMOS CTRL_OUT[5] net6 VDD VDD pfet_03v3 L=0.28u W=12.44u nf=1 ad='int((nf+1)/2) * W/nf * 0.18u'
+ as='int((nf+2)/2) * W/nf * 0.18u' pd='2*int((nf+1)/2) * (W/nf + 0.18u)' ps='2*int((nf+2)/2) * (W/nf + 0.18u)'
+ nrd='0.18u / W' nrs='0.18u / W' sa=0 sb=0 sd=0 m=1
XDCTRL_CH7_INV1_NMOS net7 CTRL_IN[7] GND GND nfet_03v3 L=0.28u W=2.34u nf=1 ad='int((nf+1)/2) * W/nf * 0.18u'
+ as='int((nf+2)/2) * W/nf * 0.18u' pd='2*int((nf+1)/2) * (W/nf + 0.18u)' ps='2*int((nf+2)/2) * (W/nf + 0.18u)'
+ nrd='0.18u / W' nrs='0.18u / W' sa=0 sb=0 sd=0 m=1
XDCTRL_CH7_INV1_PMOS net7 CTRL_IN[7] VDD VDD pfet_03v3 L=0.28u W=4.67u nf=1 ad='int((nf+1)/2) * W/nf * 0.18u'
+ as='int((nf+2)/2) * W/nf * 0.18u' pd='2*int((nf+1)/2) * (W/nf + 0.18u)' ps='2*int((nf+2)/2) * (W/nf + 0.18u)'
+ nrd='0.18u / W' nrs='0.18u / W' sa=0 sb=0 sd=0 m=1
XDCTRL_CH7_INV2_NMOS CTRL_OUT[7] net7 GND GND nfet_03v3 L=0.28u W=6.22u nf=1 ad='int((nf+1)/2) * W/nf * 0.18u'
+ as='int((nf+2)/2) * W/nf * 0.18u' pd='2*int((nf+1)/2) * (W/nf + 0.18u)' ps='2*int((nf+2)/2) * (W/nf + 0.18u)'
+ nrd='0.18u / W' nrs='0.18u / W' sa=0 sb=0 sd=0 m=1
XDCTRL_CH7_INV2_PMOS CTRL_OUT[7] net7 VDD VDD pfet_03v3 L=0.28u W=12.44u nf=1 ad='int((nf+1)/2) * W/nf * 0.18u'
+ as='int((nf+2)/2) * W/nf * 0.18u' pd='2*int((nf+1)/2) * (W/nf + 0.18u)' ps='2*int((nf+2)/2) * (W/nf + 0.18u)'
+ nrd='0.18u / W' nrs='0.18u / W' sa=0 sb=0 sd=0 m=1
.ends


* expanding   symbol:  A44_CAP_SWITCH.sym # of pins=6
** sym_path: verification/a44_w5p29_trans_driver/01_CURRENT_CIRCUIT_FILES/xschem/A44_CAP_SWITCH.sym
** sch_path: verification/a44_w5p29_trans_driver/01_CURRENT_CIRCUIT_FILES/xschem/A44_CAP_SWITCH.sch
.subckt A44_CAP_SWITCH VREFP VREFN CTRL CAP_BOTTOM VDD GND
*.iopin VREFP
*.iopin VREFN
*.ipin CTRL
*.opin CAP_BOTTOM
*.iopin VDD
*.iopin GND
XCAP_REFN_SWITCH_NMOS CAP_BOTTOM CTRL VREFN GND nfet_03v3 L=0.28u W=1.56u nf=1 ad='int((nf+1)/2) * W/nf * 0.18u'
+ as='int((nf+2)/2) * W/nf * 0.18u' pd='2*int((nf+1)/2) * (W/nf + 0.18u)' ps='2*int((nf+2)/2) * (W/nf + 0.18u)'
+ nrd='0.18u / W' nrs='0.18u / W' sa=0 sb=0 sd=0 m=18
XCAP_REFP_SWITCH_PMOS CAP_BOTTOM CTRL VREFP VDD pfet_03v3 L=0.28u W=1.56u nf=1 ad='int((nf+1)/2) * W/nf * 0.18u'
+ as='int((nf+2)/2) * W/nf * 0.18u' pd='2*int((nf+1)/2) * (W/nf + 0.18u)' ps='2*int((nf+2)/2) * (W/nf + 0.18u)'
+ nrd='0.18u / W' nrs='0.18u / W' sa=0 sb=0 sd=0 m=18
.ends

.end
